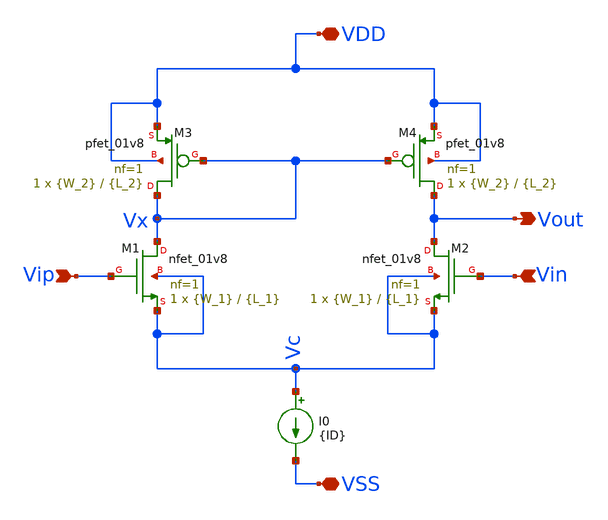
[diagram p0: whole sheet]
** sch_path: Xschem Simulations/5T-OTA/5t-ota.sch
**.subckt 5t-ota Vin Vip Vout VDD VSS
*.ipin Vin
*.ipin Vip
*.opin Vout
*.iopin VDD
*.iopin VSS
XM1 Vx Vip Vc Vc sky130_fd_pr__nfet_01v8 L={L_1} W={W_1} nf=1 ad='int((1 + 1)/2) * {W_1} / 1 * 0.29'
+ as='int((1 + 2)/2) * {W_1} / 1 * 0.29' pd='2*int((1 + 1)/2) * ({W_1} / 1 + 0.29)' ps='2*int((1 + 2)/2) * ({W_1} / 1 + 0.29)'
+ nrd='0.29 / {W_1} ' nrs='0.29 / {W_1} ' sa=0 sb=0 sd=0 mult=1 m=1
XM2 Vout Vin Vc Vc sky130_fd_pr__nfet_01v8 L={L_1} W={W_1} nf=1 ad='int((1 + 1)/2) * {W_1} / 1 * 0.29'
+ as='int((1 + 2)/2) * {W_1} / 1 * 0.29' pd='2*int((1 + 1)/2) * ({W_1} / 1 + 0.29)' ps='2*int((1 + 2)/2) * ({W_1} / 1 + 0.29)'
+ nrd='0.29 / {W_1} ' nrs='0.29 / {W_1} ' sa=0 sb=0 sd=0 mult=1 m=1
I0 Vc VSS {ID}
XM3 Vx Vx VDD VDD sky130_fd_pr__pfet_01v8 L={L_2} W={W_2} nf=1 ad='int((1 + 1)/2) * {W_2} / 1 * 0.29'
+ as='int((1 + 2)/2) * {W_2} / 1 * 0.29' pd='2*int((1 + 1)/2) * ({W_2} / 1 + 0.29)' ps='2*int((1 + 2)/2) * ({W_2} / 1 + 0.29)'
+ nrd='0.29 / {W_2} ' nrs='0.29 / {W_2} ' sa=0 sb=0 sd=0 mult=1 m=1
XM4 Vout Vx VDD VDD sky130_fd_pr__pfet_01v8 L={L_2} W={W_2} nf=1 ad='int((1 + 1)/2) * {W_2} / 1 * 0.29'
+ as='int((1 + 2)/2) * {W_2} / 1 * 0.29' pd='2*int((1 + 1)/2) * ({W_2} / 1 + 0.29)' ps='2*int((1 + 2)/2) * ({W_2} / 1 + 0.29)'
+ nrd='0.29 / {W_2} ' nrs='0.29 / {W_2} ' sa=0 sb=0 sd=0 mult=1 m=1
**** begin user architecture code

** opencircuitdesign pdks install
.lib $::SKYWATER_MODELS/sky130.lib.spice tt

**** end user architecture code
**.ends
.end
